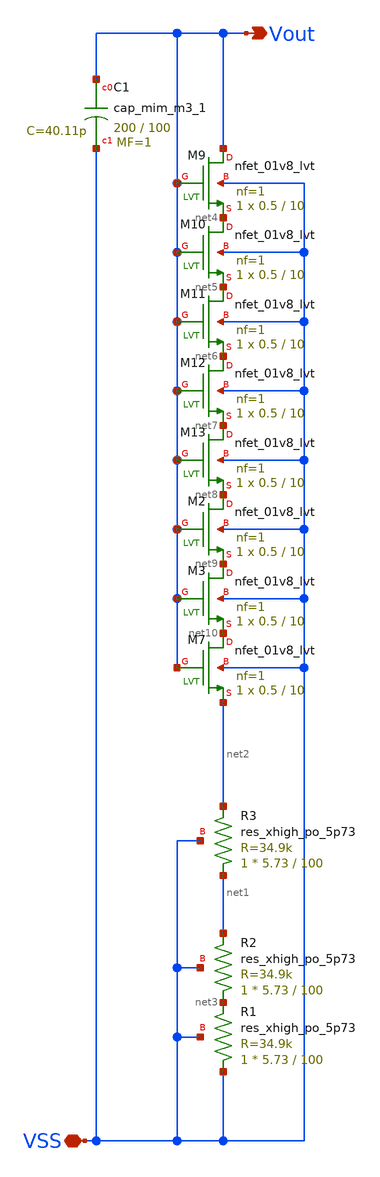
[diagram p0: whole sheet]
** sch_path: xschem/cmos_imager/photodiode_real_rc_40p.sch
**.subckt photodiode_real_rc_40p Vout VSS
*.opin Vout
*.iopin VSS
XC1 Vout VSS sky130_fd_pr__cap_mim_m3_1 W=200 L=100 MF=1 m=1
XR1 VSS net3 VSS sky130_fd_pr__res_xhigh_po_5p73 L=100 mult=1 m=1
XR2 net3 net1 VSS sky130_fd_pr__res_xhigh_po_5p73 L=100 mult=1 m=1
XM9 Vout Vout net4 VSS sky130_fd_pr__nfet_01v8_lvt L=10 W=0.5 nf=1 ad='int((nf+1)/2) * W/nf * 0.29' as='int((nf+2)/2) * W/nf * 0.29'
+ pd='2*int((nf+1)/2) * (W/nf + 0.29)' ps='2*int((nf+2)/2) * (W/nf + 0.29)' nrd='0.29 / W' nrs='0.29 / W'
+ sa=0 sb=0 sd=0 mult=1 m=1
XM10 net4 Vout net5 VSS sky130_fd_pr__nfet_01v8_lvt L=10 W=0.5 nf=1 ad='int((nf+1)/2) * W/nf * 0.29'
+ as='int((nf+2)/2) * W/nf * 0.29' pd='2*int((nf+1)/2) * (W/nf + 0.29)' ps='2*int((nf+2)/2) * (W/nf + 0.29)'
+ nrd='0.29 / W' nrs='0.29 / W' sa=0 sb=0 sd=0 mult=1 m=1
XM11 net5 Vout net6 VSS sky130_fd_pr__nfet_01v8_lvt L=10 W=0.5 nf=1 ad='int((nf+1)/2) * W/nf * 0.29'
+ as='int((nf+2)/2) * W/nf * 0.29' pd='2*int((nf+1)/2) * (W/nf + 0.29)' ps='2*int((nf+2)/2) * (W/nf + 0.29)'
+ nrd='0.29 / W' nrs='0.29 / W' sa=0 sb=0 sd=0 mult=1 m=1
XM12 net6 Vout net7 VSS sky130_fd_pr__nfet_01v8_lvt L=10 W=0.5 nf=1 ad='int((nf+1)/2) * W/nf * 0.29'
+ as='int((nf+2)/2) * W/nf * 0.29' pd='2*int((nf+1)/2) * (W/nf + 0.29)' ps='2*int((nf+2)/2) * (W/nf + 0.29)'
+ nrd='0.29 / W' nrs='0.29 / W' sa=0 sb=0 sd=0 mult=1 m=1
XM13 net7 Vout net8 VSS sky130_fd_pr__nfet_01v8_lvt L=10 W=0.5 nf=1 ad='int((nf+1)/2) * W/nf * 0.29'
+ as='int((nf+2)/2) * W/nf * 0.29' pd='2*int((nf+1)/2) * (W/nf + 0.29)' ps='2*int((nf+2)/2) * (W/nf + 0.29)'
+ nrd='0.29 / W' nrs='0.29 / W' sa=0 sb=0 sd=0 mult=1 m=1
XM2 net8 Vout net9 VSS sky130_fd_pr__nfet_01v8_lvt L=10 W=0.5 nf=1 ad='int((nf+1)/2) * W/nf * 0.29' as='int((nf+2)/2) * W/nf * 0.29'
+ pd='2*int((nf+1)/2) * (W/nf + 0.29)' ps='2*int((nf+2)/2) * (W/nf + 0.29)' nrd='0.29 / W' nrs='0.29 / W'
+ sa=0 sb=0 sd=0 mult=1 m=1
XM3 net9 Vout net10 VSS sky130_fd_pr__nfet_01v8_lvt L=10 W=0.5 nf=1 ad='int((nf+1)/2) * W/nf * 0.29'
+ as='int((nf+2)/2) * W/nf * 0.29' pd='2*int((nf+1)/2) * (W/nf + 0.29)' ps='2*int((nf+2)/2) * (W/nf + 0.29)'
+ nrd='0.29 / W' nrs='0.29 / W' sa=0 sb=0 sd=0 mult=1 m=1
XM7 net10 Vout net2 VSS sky130_fd_pr__nfet_01v8_lvt L=10 W=0.5 nf=1 ad='int((nf+1)/2) * W/nf * 0.29'
+ as='int((nf+2)/2) * W/nf * 0.29' pd='2*int((nf+1)/2) * (W/nf + 0.29)' ps='2*int((nf+2)/2) * (W/nf + 0.29)'
+ nrd='0.29 / W' nrs='0.29 / W' sa=0 sb=0 sd=0 mult=1 m=1
XR3 net1 net2 VSS sky130_fd_pr__res_xhigh_po_5p73 L=100 mult=1 m=1
**.ends
.end
